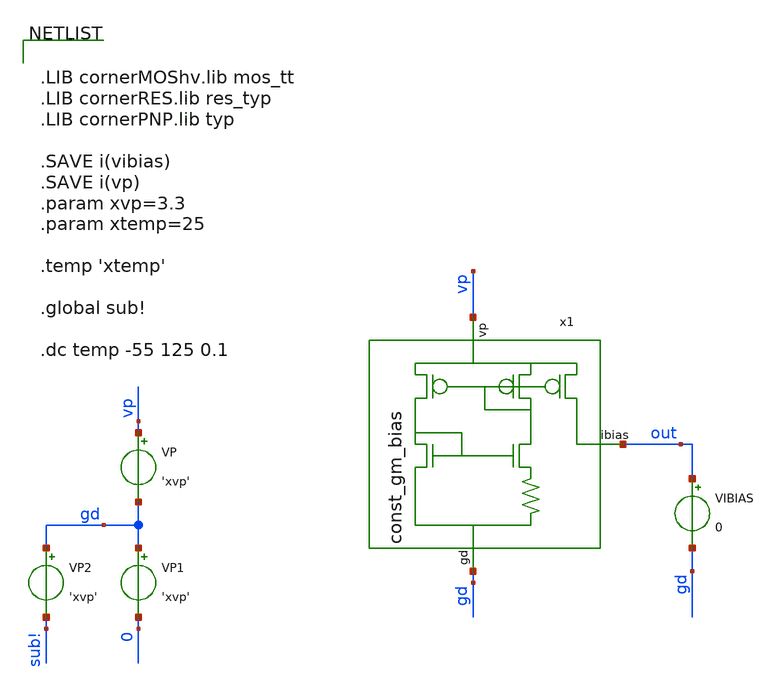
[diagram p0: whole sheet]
** sch_path: testbench/const_gm_bias_temp_sweep_tb.sch
**.subckt const_gm_bias_temp_sweep_tb
x1 vp out gd const_gm_bias
VP vp gd 'xvp'
.save i(vp)
VP1 gd 0 'xvp'
VP2 gd sub! 'xvp'
VIBIAS out gd 0
.save i(vibias)
**** begin user architecture code


.LIB cornerMOShv.lib mos_tt
.LIB cornerRES.lib res_typ
.LIB cornerPNP.lib typ

.SAVE i(vibias)
.SAVE i(vp)
.param xvp=3.3
.param xtemp=25

.temp 'xtemp'

.global sub!

.dc temp -55 125 0.1


**** end user architecture code
**.ends
.end
